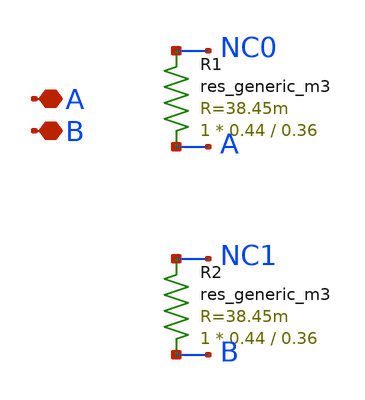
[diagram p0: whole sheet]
** sch_path: ip/sun_tr_sky130nm/design/SUN_TR_SKY130NM/SUNTR_CAPBASE_LEFT_SIDE_PORT.sch
**.subckt SUNTR_CAPBASE_LEFT_SIDE_PORT A B
*.iopin A
*.iopin B
R1 A NC0 sky130_fd_pr__res_generic_m3 W=0.44 L=0.36 m=1
R2 B NC1 sky130_fd_pr__res_generic_m3 W=0.44 L=0.36 m=1
**.ends
.end
